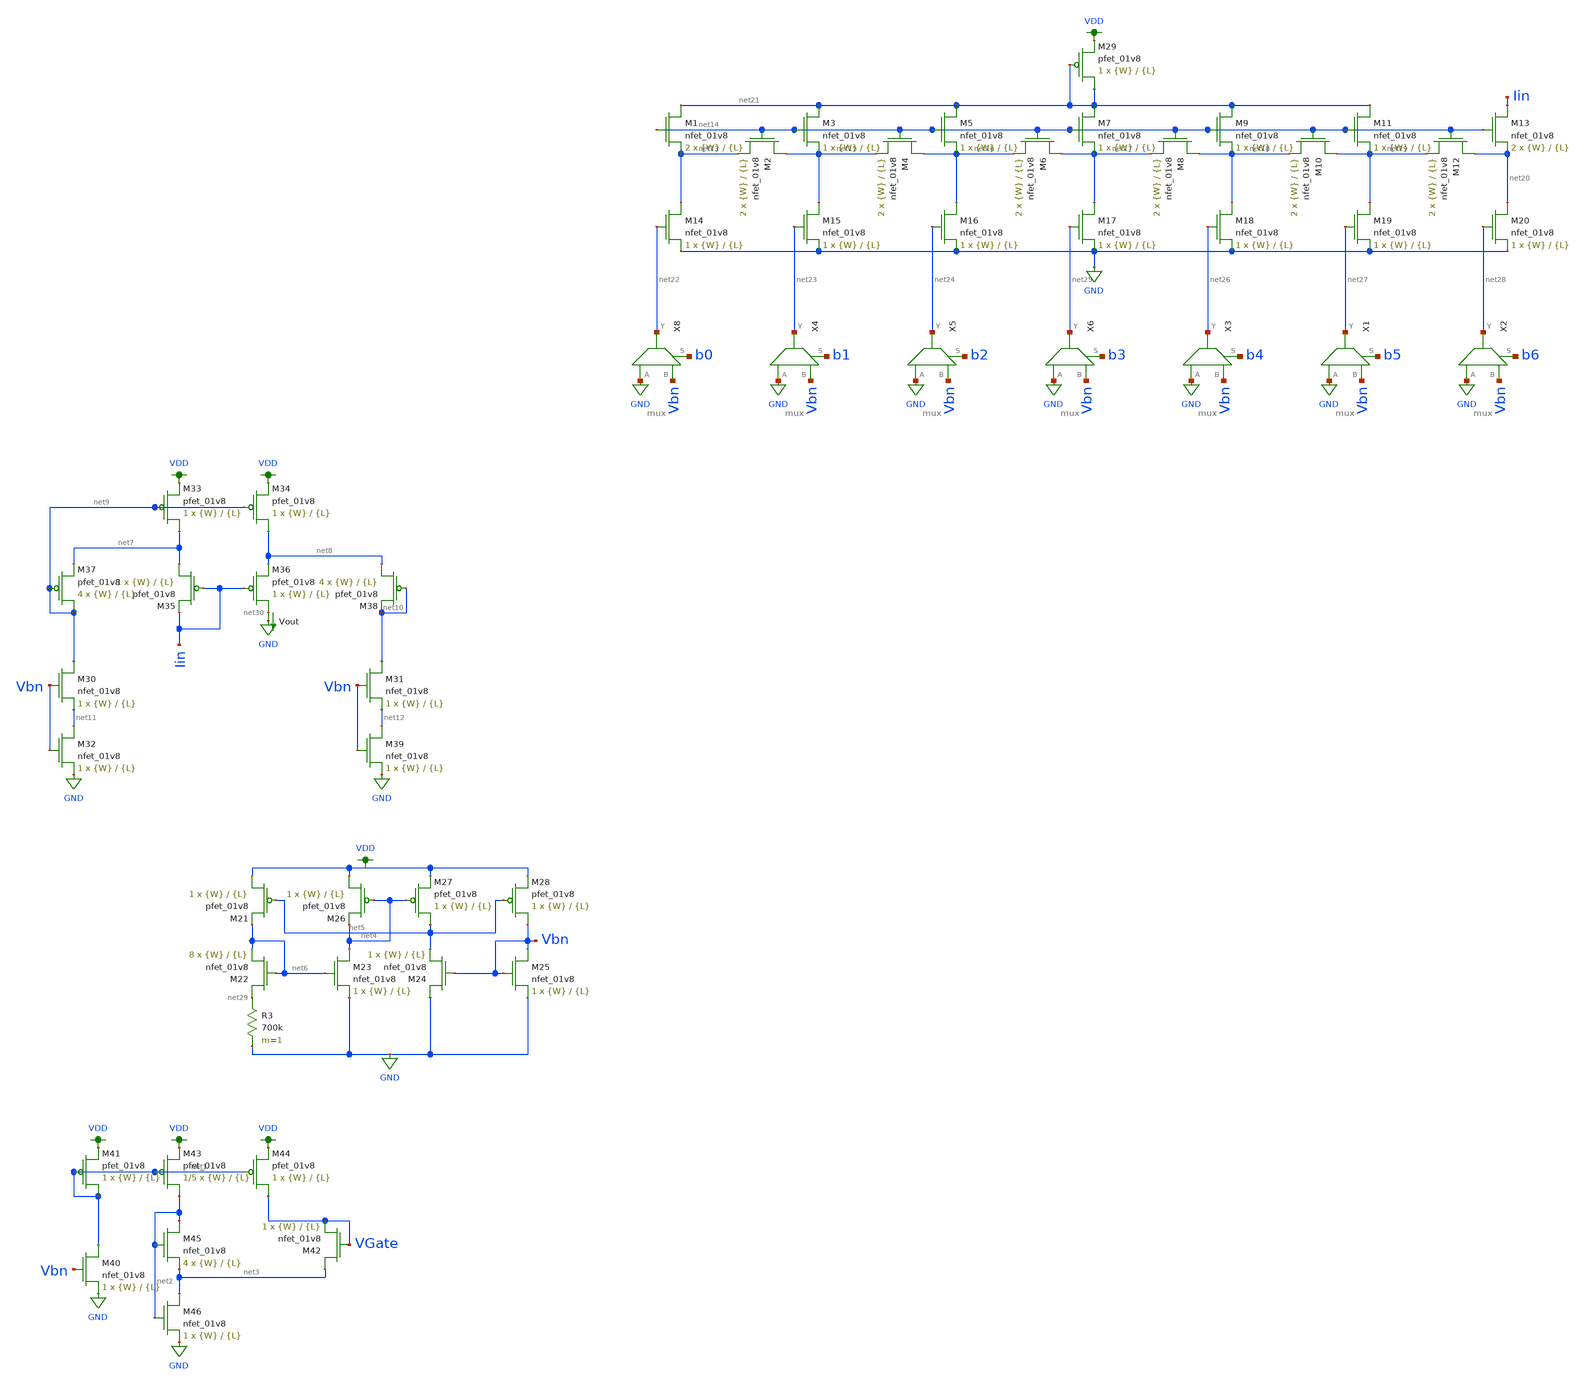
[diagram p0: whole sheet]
** sch_path: dac/schematics/misc/untitled-1.sch
**.subckt untitled-1
XM40 net1 Vbn GND GND sky130_fd_pr__nfet_01v8 L={L} W={W} nf=1 ad='int((nf+1)/2) * W/nf * 0.29' as='int((nf+2)/2) * W/nf * 0.29'
+ pd='2*int((nf+1)/2) * (W/nf + 0.29)' ps='2*int((nf+2)/2) * (W/nf + 0.29)' nrd='0.29 / W' nrs='0.29 / W'
+ sa=0 sb=0 sd=0 mult=1 m=1
XM41 net1 net1 VDD VDD sky130_fd_pr__pfet_01v8 L={L} W={W} nf=1 ad='int((nf+1)/2) * W/nf * 0.29' as='int((nf+2)/2) * W/nf * 0.29'
+ pd='2*int((nf+1)/2) * (W/nf + 0.29)' ps='2*int((nf+2)/2) * (W/nf + 0.29)' nrd='0.29 / W' nrs='0.29 / W'
+ sa=0 sb=0 sd=0 mult=1 m=1
XM42 net3 VGate VGate GND sky130_fd_pr__nfet_01v8 L={L} W={W} nf=1 ad='int((nf+1)/2) * W/nf * 0.29' as='int((nf+2)/2) * W/nf * 0.29'
+ pd='2*int((nf+1)/2) * (W/nf + 0.29)' ps='2*int((nf+2)/2) * (W/nf + 0.29)' nrd='0.29 / W' nrs='0.29 / W'
+ sa=0 sb=0 sd=0 mult=1 m=1
XM43 net2 net1 VDD VDD sky130_fd_pr__pfet_01v8 L={L} W={W} nf=1 ad='int((nf+1)/2) * W/nf * 0.29' as='int((nf+2)/2) * W/nf * 0.29'
+ pd='2*int((nf+1)/2) * (W/nf + 0.29)' ps='2*int((nf+2)/2) * (W/nf + 0.29)' nrd='0.29 / W' nrs='0.29 / W'
+ sa=0 sb=0 sd=0 mult=1/5 m=1/5
XM44 VGate net1 VDD VDD sky130_fd_pr__pfet_01v8 L={L} W={W} nf=1 ad='int((nf+1)/2) * W/nf * 0.29' as='int((nf+2)/2) * W/nf * 0.29'
+ pd='2*int((nf+1)/2) * (W/nf + 0.29)' ps='2*int((nf+2)/2) * (W/nf + 0.29)' nrd='0.29 / W' nrs='0.29 / W'
+ sa=0 sb=0 sd=0 mult=1 m=1
XM45 net2 net2 net3 GND sky130_fd_pr__nfet_01v8 L={L} W={W} nf=1 ad='int((nf+1)/2) * W/nf * 0.29' as='int((nf+2)/2) * W/nf * 0.29'
+ pd='2*int((nf+1)/2) * (W/nf + 0.29)' ps='2*int((nf+2)/2) * (W/nf + 0.29)' nrd='0.29 / W' nrs='0.29 / W'
+ sa=0 sb=0 sd=0 mult=4 m=4
XM46 net3 net2 GND GND sky130_fd_pr__nfet_01v8 L={L} W={W} nf=1 ad='int((nf+1)/2) * W/nf * 0.29' as='int((nf+2)/2) * W/nf * 0.29'
+ pd='2*int((nf+1)/2) * (W/nf + 0.29)' ps='2*int((nf+2)/2) * (W/nf + 0.29)' nrd='0.29 / W' nrs='0.29 / W'
+ sa=0 sb=0 sd=0 mult=1 m=1
XM21 VDD net5 net6 VDD sky130_fd_pr__pfet_01v8 L={L} W={W} nf=1 ad='int((nf+1)/2) * W/nf * 0.29' as='int((nf+2)/2) * W/nf * 0.29'
+ pd='2*int((nf+1)/2) * (W/nf + 0.29)' ps='2*int((nf+2)/2) * (W/nf + 0.29)' nrd='0.29 / W' nrs='0.29 / W'
+ sa=0 sb=0 sd=0 mult=1 m=1
XM22 net29 net6 net6 GND sky130_fd_pr__nfet_01v8 L={L} W={W} nf=1 ad='int((nf+1)/2) * W/nf * 0.29' as='int((nf+2)/2) * W/nf * 0.29'
+ pd='2*int((nf+1)/2) * (W/nf + 0.29)' ps='2*int((nf+2)/2) * (W/nf + 0.29)' nrd='0.29 / W' nrs='0.29 / W'
+ sa=0 sb=0 sd=0 mult=8 m=8
R3 net29 GND 700k m=1
XM23 net4 net6 GND GND sky130_fd_pr__nfet_01v8 L={L} W={W} nf=1 ad='int((nf+1)/2) * W/nf * 0.29' as='int((nf+2)/2) * W/nf * 0.29'
+ pd='2*int((nf+1)/2) * (W/nf + 0.29)' ps='2*int((nf+2)/2) * (W/nf + 0.29)' nrd='0.29 / W' nrs='0.29 / W'
+ sa=0 sb=0 sd=0 mult=1 m=1
XM24 GND Vbn net5 GND sky130_fd_pr__nfet_01v8 L={L} W={W} nf=1 ad='int((nf+1)/2) * W/nf * 0.29' as='int((nf+2)/2) * W/nf * 0.29'
+ pd='2*int((nf+1)/2) * (W/nf + 0.29)' ps='2*int((nf+2)/2) * (W/nf + 0.29)' nrd='0.29 / W' nrs='0.29 / W'
+ sa=0 sb=0 sd=0 mult=1 m=1
XM25 Vbn Vbn GND GND sky130_fd_pr__nfet_01v8 L={L} W={W} nf=1 ad='int((nf+1)/2) * W/nf * 0.29' as='int((nf+2)/2) * W/nf * 0.29'
+ pd='2*int((nf+1)/2) * (W/nf + 0.29)' ps='2*int((nf+2)/2) * (W/nf + 0.29)' nrd='0.29 / W' nrs='0.29 / W'
+ sa=0 sb=0 sd=0 mult=1 m=1
XM26 VDD net4 net4 VDD sky130_fd_pr__pfet_01v8 L={L} W={W} nf=1 ad='int((nf+1)/2) * W/nf * 0.29' as='int((nf+2)/2) * W/nf * 0.29'
+ pd='2*int((nf+1)/2) * (W/nf + 0.29)' ps='2*int((nf+2)/2) * (W/nf + 0.29)' nrd='0.29 / W' nrs='0.29 / W'
+ sa=0 sb=0 sd=0 mult=1 m=1
XM27 net5 net4 VDD VDD sky130_fd_pr__pfet_01v8 L={L} W={W} nf=1 ad='int((nf+1)/2) * W/nf * 0.29' as='int((nf+2)/2) * W/nf * 0.29'
+ pd='2*int((nf+1)/2) * (W/nf + 0.29)' ps='2*int((nf+2)/2) * (W/nf + 0.29)' nrd='0.29 / W' nrs='0.29 / W'
+ sa=0 sb=0 sd=0 mult=1 m=1
XM28 Vbn net5 VDD VDD sky130_fd_pr__pfet_01v8 L={L} W={W} nf=1 ad='int((nf+1)/2) * W/nf * 0.29' as='int((nf+2)/2) * W/nf * 0.29'
+ pd='2*int((nf+1)/2) * (W/nf + 0.29)' ps='2*int((nf+2)/2) * (W/nf + 0.29)' nrd='0.29 / W' nrs='0.29 / W'
+ sa=0 sb=0 sd=0 mult=1 m=1
Vout net30 GND 0
.save i(vout)
XM33 net7 net9 VDD VDD sky130_fd_pr__pfet_01v8 L={L} W={W} nf=1 ad='int((nf+1)/2) * W/nf * 0.29' as='int((nf+2)/2) * W/nf * 0.29'
+ pd='2*int((nf+1)/2) * (W/nf + 0.29)' ps='2*int((nf+2)/2) * (W/nf + 0.29)' nrd='0.29 / W' nrs='0.29 / W'
+ sa=0 sb=0 sd=0 mult=1 m=1
XM34 net8 net9 VDD VDD sky130_fd_pr__pfet_01v8 L={L} W={W} nf=1 ad='int((nf+1)/2) * W/nf * 0.29' as='int((nf+2)/2) * W/nf * 0.29'
+ pd='2*int((nf+1)/2) * (W/nf + 0.29)' ps='2*int((nf+2)/2) * (W/nf + 0.29)' nrd='0.29 / W' nrs='0.29 / W'
+ sa=0 sb=0 sd=0 mult=1 m=1
XM35 net7 Iin Iin VDD sky130_fd_pr__pfet_01v8 L={L} W={W} nf=1 ad='int((nf+1)/2) * W/nf * 0.29' as='int((nf+2)/2) * W/nf * 0.29'
+ pd='2*int((nf+1)/2) * (W/nf + 0.29)' ps='2*int((nf+2)/2) * (W/nf + 0.29)' nrd='0.29 / W' nrs='0.29 / W'
+ sa=0 sb=0 sd=0 mult=1 m=1
XM36 net30 Iin net8 VDD sky130_fd_pr__pfet_01v8 L={L} W={W} nf=1 ad='int((nf+1)/2) * W/nf * 0.29' as='int((nf+2)/2) * W/nf * 0.29'
+ pd='2*int((nf+1)/2) * (W/nf + 0.29)' ps='2*int((nf+2)/2) * (W/nf + 0.29)' nrd='0.29 / W' nrs='0.29 / W'
+ sa=0 sb=0 sd=0 mult=1 m=1
XM37 net9 net9 net7 VDD sky130_fd_pr__pfet_01v8 L={L} W={W} nf=1 ad='int((nf+1)/2) * W/nf * 0.29' as='int((nf+2)/2) * W/nf * 0.29'
+ pd='2*int((nf+1)/2) * (W/nf + 0.29)' ps='2*int((nf+2)/2) * (W/nf + 0.29)' nrd='0.29 / W' nrs='0.29 / W'
+ sa=0 sb=0 sd=0 mult=4 m=4
XM38 net8 net10 net10 VDD sky130_fd_pr__pfet_01v8 L={L} W={W} nf=1 ad='int((nf+1)/2) * W/nf * 0.29' as='int((nf+2)/2) * W/nf * 0.29'
+ pd='2*int((nf+1)/2) * (W/nf + 0.29)' ps='2*int((nf+2)/2) * (W/nf + 0.29)' nrd='0.29 / W' nrs='0.29 / W'
+ sa=0 sb=0 sd=0 mult=4 m=4
XM30 net9 Vbn net11 GND sky130_fd_pr__nfet_01v8 L={L} W={W} nf=1 ad='int((nf+1)/2) * W/nf * 0.29' as='int((nf+2)/2) * W/nf * 0.29'
+ pd='2*int((nf+1)/2) * (W/nf + 0.29)' ps='2*int((nf+2)/2) * (W/nf + 0.29)' nrd='0.29 / W' nrs='0.29 / W'
+ sa=0 sb=0 sd=0 mult=1 m=1
XM31 net10 Vbn net12 GND sky130_fd_pr__nfet_01v8 L={L} W={W} nf=1 ad='int((nf+1)/2) * W/nf * 0.29' as='int((nf+2)/2) * W/nf * 0.29'
+ pd='2*int((nf+1)/2) * (W/nf + 0.29)' ps='2*int((nf+2)/2) * (W/nf + 0.29)' nrd='0.29 / W' nrs='0.29 / W'
+ sa=0 sb=0 sd=0 mult=1 m=1
XM32 net11 Vbn GND GND sky130_fd_pr__nfet_01v8 L={L} W={W} nf=1 ad='int((nf+1)/2) * W/nf * 0.29' as='int((nf+2)/2) * W/nf * 0.29'
+ pd='2*int((nf+1)/2) * (W/nf + 0.29)' ps='2*int((nf+2)/2) * (W/nf + 0.29)' nrd='0.29 / W' nrs='0.29 / W'
+ sa=0 sb=0 sd=0 mult=1 m=1
XM39 net12 Vbn GND GND sky130_fd_pr__nfet_01v8 L={L} W={W} nf=1 ad='int((nf+1)/2) * W/nf * 0.29' as='int((nf+2)/2) * W/nf * 0.29'
+ pd='2*int((nf+1)/2) * (W/nf + 0.29)' ps='2*int((nf+2)/2) * (W/nf + 0.29)' nrd='0.29 / W' nrs='0.29 / W'
+ sa=0 sb=0 sd=0 mult=1 m=1
XM1 net21 net14 net13 GND sky130_fd_pr__nfet_01v8 L={L} W={W} nf=1 ad='int((nf+1)/2) * W/nf * 0.29' as='int((nf+2)/2) * W/nf * 0.29'
+ pd='2*int((nf+1)/2) * (W/nf + 0.29)' ps='2*int((nf+2)/2) * (W/nf + 0.29)' nrd='0.29 / W' nrs='0.29 / W'
+ sa=0 sb=0 sd=0 mult=2 m=2
XM2 net15 net14 net13 GND sky130_fd_pr__nfet_01v8 L={L} W={W} nf=1 ad='int((nf+1)/2) * W/nf * 0.29' as='int((nf+2)/2) * W/nf * 0.29'
+ pd='2*int((nf+1)/2) * (W/nf + 0.29)' ps='2*int((nf+2)/2) * (W/nf + 0.29)' nrd='0.29 / W' nrs='0.29 / W'
+ sa=0 sb=0 sd=0 mult=2 m=2
XM3 net21 net14 net15 GND sky130_fd_pr__nfet_01v8 L={L} W={W} nf=1 ad='int((nf+1)/2) * W/nf * 0.29' as='int((nf+2)/2) * W/nf * 0.29'
+ pd='2*int((nf+1)/2) * (W/nf + 0.29)' ps='2*int((nf+2)/2) * (W/nf + 0.29)' nrd='0.29 / W' nrs='0.29 / W'
+ sa=0 sb=0 sd=0 mult=1 m=1
XM4 net16 net14 net15 GND sky130_fd_pr__nfet_01v8 L={L} W={W} nf=1 ad='int((nf+1)/2) * W/nf * 0.29' as='int((nf+2)/2) * W/nf * 0.29'
+ pd='2*int((nf+1)/2) * (W/nf + 0.29)' ps='2*int((nf+2)/2) * (W/nf + 0.29)' nrd='0.29 / W' nrs='0.29 / W'
+ sa=0 sb=0 sd=0 mult=2 m=2
XM5 net21 net14 net16 GND sky130_fd_pr__nfet_01v8 L={L} W={W} nf=1 ad='int((nf+1)/2) * W/nf * 0.29' as='int((nf+2)/2) * W/nf * 0.29'
+ pd='2*int((nf+1)/2) * (W/nf + 0.29)' ps='2*int((nf+2)/2) * (W/nf + 0.29)' nrd='0.29 / W' nrs='0.29 / W'
+ sa=0 sb=0 sd=0 mult=1 m=1
XM6 net17 net14 net16 GND sky130_fd_pr__nfet_01v8 L={L} W={W} nf=1 ad='int((nf+1)/2) * W/nf * 0.29' as='int((nf+2)/2) * W/nf * 0.29'
+ pd='2*int((nf+1)/2) * (W/nf + 0.29)' ps='2*int((nf+2)/2) * (W/nf + 0.29)' nrd='0.29 / W' nrs='0.29 / W'
+ sa=0 sb=0 sd=0 mult=2 m=2
XM7 net21 net14 net17 GND sky130_fd_pr__nfet_01v8 L={L} W={W} nf=1 ad='int((nf+1)/2) * W/nf * 0.29' as='int((nf+2)/2) * W/nf * 0.29'
+ pd='2*int((nf+1)/2) * (W/nf + 0.29)' ps='2*int((nf+2)/2) * (W/nf + 0.29)' nrd='0.29 / W' nrs='0.29 / W'
+ sa=0 sb=0 sd=0 mult=1 m=1
XM8 net18 net14 net17 GND sky130_fd_pr__nfet_01v8 L={L} W={W} nf=1 ad='int((nf+1)/2) * W/nf * 0.29' as='int((nf+2)/2) * W/nf * 0.29'
+ pd='2*int((nf+1)/2) * (W/nf + 0.29)' ps='2*int((nf+2)/2) * (W/nf + 0.29)' nrd='0.29 / W' nrs='0.29 / W'
+ sa=0 sb=0 sd=0 mult=2 m=2
XM9 net21 net14 net18 GND sky130_fd_pr__nfet_01v8 L={L} W={W} nf=1 ad='int((nf+1)/2) * W/nf * 0.29' as='int((nf+2)/2) * W/nf * 0.29'
+ pd='2*int((nf+1)/2) * (W/nf + 0.29)' ps='2*int((nf+2)/2) * (W/nf + 0.29)' nrd='0.29 / W' nrs='0.29 / W'
+ sa=0 sb=0 sd=0 mult=1 m=1
XM10 net19 net14 net18 GND sky130_fd_pr__nfet_01v8 L={L} W={W} nf=1 ad='int((nf+1)/2) * W/nf * 0.29'
+ as='int((nf+2)/2) * W/nf * 0.29' pd='2*int((nf+1)/2) * (W/nf + 0.29)' ps='2*int((nf+2)/2) * (W/nf + 0.29)'
+ nrd='0.29 / W' nrs='0.29 / W' sa=0 sb=0 sd=0 mult=2 m=2
XM11 net21 net14 net19 GND sky130_fd_pr__nfet_01v8 L={L} W={W} nf=1 ad='int((nf+1)/2) * W/nf * 0.29'
+ as='int((nf+2)/2) * W/nf * 0.29' pd='2*int((nf+1)/2) * (W/nf + 0.29)' ps='2*int((nf+2)/2) * (W/nf + 0.29)'
+ nrd='0.29 / W' nrs='0.29 / W' sa=0 sb=0 sd=0 mult=1 m=1
XM12 net20 net14 net19 GND sky130_fd_pr__nfet_01v8 L={L} W={W} nf=1 ad='int((nf+1)/2) * W/nf * 0.29'
+ as='int((nf+2)/2) * W/nf * 0.29' pd='2*int((nf+1)/2) * (W/nf + 0.29)' ps='2*int((nf+2)/2) * (W/nf + 0.29)'
+ nrd='0.29 / W' nrs='0.29 / W' sa=0 sb=0 sd=0 mult=2 m=2
XM13 Iin net14 net20 GND sky130_fd_pr__nfet_01v8 L={L} W={W} nf=1 ad='int((nf+1)/2) * W/nf * 0.29' as='int((nf+2)/2) * W/nf * 0.29'
+ pd='2*int((nf+1)/2) * (W/nf + 0.29)' ps='2*int((nf+2)/2) * (W/nf + 0.29)' nrd='0.29 / W' nrs='0.29 / W'
+ sa=0 sb=0 sd=0 mult=2 m=2
XM14 net13 net22 GND GND sky130_fd_pr__nfet_01v8 L={L} W={W} nf=1 ad='int((nf+1)/2) * W/nf * 0.29' as='int((nf+2)/2) * W/nf * 0.29'
+ pd='2*int((nf+1)/2) * (W/nf + 0.29)' ps='2*int((nf+2)/2) * (W/nf + 0.29)' nrd='0.29 / W' nrs='0.29 / W'
+ sa=0 sb=0 sd=0 mult=1 m=1
XM15 net15 net23 GND GND sky130_fd_pr__nfet_01v8 L={L} W={W} nf=1 ad='int((nf+1)/2) * W/nf * 0.29' as='int((nf+2)/2) * W/nf * 0.29'
+ pd='2*int((nf+1)/2) * (W/nf + 0.29)' ps='2*int((nf+2)/2) * (W/nf + 0.29)' nrd='0.29 / W' nrs='0.29 / W'
+ sa=0 sb=0 sd=0 mult=1 m=1
XM16 net16 net24 GND GND sky130_fd_pr__nfet_01v8 L={L} W={W} nf=1 ad='int((nf+1)/2) * W/nf * 0.29' as='int((nf+2)/2) * W/nf * 0.29'
+ pd='2*int((nf+1)/2) * (W/nf + 0.29)' ps='2*int((nf+2)/2) * (W/nf + 0.29)' nrd='0.29 / W' nrs='0.29 / W'
+ sa=0 sb=0 sd=0 mult=1 m=1
XM17 net17 net25 GND GND sky130_fd_pr__nfet_01v8 L={L} W={W} nf=1 ad='int((nf+1)/2) * W/nf * 0.29' as='int((nf+2)/2) * W/nf * 0.29'
+ pd='2*int((nf+1)/2) * (W/nf + 0.29)' ps='2*int((nf+2)/2) * (W/nf + 0.29)' nrd='0.29 / W' nrs='0.29 / W'
+ sa=0 sb=0 sd=0 mult=1 m=1
XM18 net18 net26 GND GND sky130_fd_pr__nfet_01v8 L={L} W={W} nf=1 ad='int((nf+1)/2) * W/nf * 0.29' as='int((nf+2)/2) * W/nf * 0.29'
+ pd='2*int((nf+1)/2) * (W/nf + 0.29)' ps='2*int((nf+2)/2) * (W/nf + 0.29)' nrd='0.29 / W' nrs='0.29 / W'
+ sa=0 sb=0 sd=0 mult=1 m=1
XM19 net19 net27 GND GND sky130_fd_pr__nfet_01v8 L={L} W={W} nf=1 ad='int((nf+1)/2) * W/nf * 0.29' as='int((nf+2)/2) * W/nf * 0.29'
+ pd='2*int((nf+1)/2) * (W/nf + 0.29)' ps='2*int((nf+2)/2) * (W/nf + 0.29)' nrd='0.29 / W' nrs='0.29 / W'
+ sa=0 sb=0 sd=0 mult=1 m=1
XM20 net20 net28 GND GND sky130_fd_pr__nfet_01v8 L={L} W={W} nf=1 ad='int((nf+1)/2) * W/nf * 0.29' as='int((nf+2)/2) * W/nf * 0.29'
+ pd='2*int((nf+1)/2) * (W/nf + 0.29)' ps='2*int((nf+2)/2) * (W/nf + 0.29)' nrd='0.29 / W' nrs='0.29 / W'
+ sa=0 sb=0 sd=0 mult=1 m=1
XM29 net21 net21 VDD VDD sky130_fd_pr__pfet_01v8 L={L} W={W} nf=1 ad='int((nf+1)/2) * W/nf * 0.29' as='int((nf+2)/2) * W/nf * 0.29'
+ pd='2*int((nf+1)/2) * (W/nf + 0.29)' ps='2*int((nf+2)/2) * (W/nf + 0.29)' nrd='0.29 / W' nrs='0.29 / W'
+ sa=0 sb=0 sd=0 mult=1 m=1
X8 GND Vbn net22 b0 mux
X4 GND Vbn net23 b1 mux
X5 GND Vbn net24 b2 mux
X6 GND Vbn net25 b3 mux
X3 GND Vbn net26 b4 mux
X1 GND Vbn net27 b5 mux
X2 GND Vbn net28 b6 mux
**.ends

* expanding   symbol:  /home/madvlsi/Documents/current-output-dac-vlsi/schematics/mux.sym # of
*+ pins=4
** sym_path: dac/schematics/mux.sym
** sch_path: dac/schematics/mux.sch
.subckt mux A B Y S
*.ipin A
*.ipin B
*.ipin S
*.opin Y
XM1 A S Y VDD sky130_fd_pr__pfet_01v8 L=0.15 W=1 nf=1 ad='int((nf+1)/2) * W/nf * 0.29' as='int((nf+2)/2) * W/nf * 0.29'
+ pd='2*int((nf+1)/2) * (W/nf + 0.29)' ps='2*int((nf+2)/2) * (W/nf + 0.29)' nrd='0.29 / W' nrs='0.29 / W'
+ sa=0 sb=0 sd=0 mult=1 m=1
XM3 net1 S VDD VDD sky130_fd_pr__pfet_01v8 L=0.15 W=1 nf=1 ad='int((nf+1)/2) * W/nf * 0.29' as='int((nf+2)/2) * W/nf * 0.29'
+ pd='2*int((nf+1)/2) * (W/nf + 0.29)' ps='2*int((nf+2)/2) * (W/nf + 0.29)' nrd='0.29 / W' nrs='0.29 / W'
+ sa=0 sb=0 sd=0 mult=1 m=1
XM4 net1 S GND GND sky130_fd_pr__nfet_01v8 L=0.15 W=1 nf=1 ad='int((nf+1)/2) * W/nf * 0.29' as='int((nf+2)/2) * W/nf * 0.29'
+ pd='2*int((nf+1)/2) * (W/nf + 0.29)' ps='2*int((nf+2)/2) * (W/nf + 0.29)' nrd='0.29 / W' nrs='0.29 / W'
+ sa=0 sb=0 sd=0 mult=1 m=1
XM5 A net1 Y GND sky130_fd_pr__nfet_01v8 L=0.15 W=1 nf=1 ad='int((nf+1)/2) * W/nf * 0.29' as='int((nf+2)/2) * W/nf * 0.29'
+ pd='2*int((nf+1)/2) * (W/nf + 0.29)' ps='2*int((nf+2)/2) * (W/nf + 0.29)' nrd='0.29 / W' nrs='0.29 / W'
+ sa=0 sb=0 sd=0 mult=1 m=1
XM2 B net1 Y VDD sky130_fd_pr__pfet_01v8 L=0.15 W=1 nf=1 ad='int((nf+1)/2) * W/nf * 0.29' as='int((nf+2)/2) * W/nf * 0.29'
+ pd='2*int((nf+1)/2) * (W/nf + 0.29)' ps='2*int((nf+2)/2) * (W/nf + 0.29)' nrd='0.29 / W' nrs='0.29 / W'
+ sa=0 sb=0 sd=0 mult=1 m=1
XM6 B S Y GND sky130_fd_pr__nfet_01v8 L=0.15 W=1 nf=1 ad='int((nf+1)/2) * W/nf * 0.29' as='int((nf+2)/2) * W/nf * 0.29'
+ pd='2*int((nf+1)/2) * (W/nf + 0.29)' ps='2*int((nf+2)/2) * (W/nf + 0.29)' nrd='0.29 / W' nrs='0.29 / W'
+ sa=0 sb=0 sd=0 mult=1 m=1
.ends

.GLOBAL GND
.GLOBAL VDD
.end
